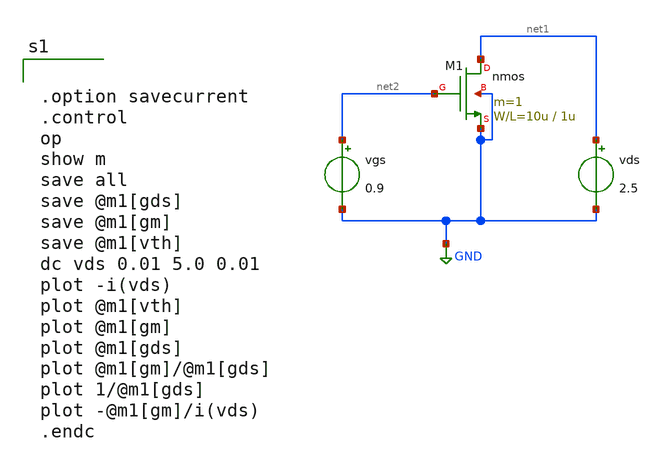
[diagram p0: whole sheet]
** sch_path: member_project/GroupWork/Team_masahiro/nfet_id-vds.sch
**.subckt nfet_id-vds
vgs net2 GND 0.9
vds net1 GND 2.5
M1 net1 net2 GND GND nmos L=1u W=10u m=1
**** begin user architecture code
 .include $::LIB/mos.lib
.include $::LIB/passive.lib
.include $::LIB/diode.lib


.option savecurrent
.control
op
show m
save all
save @m1[gds]
save @m1[gm]
save @m1[vth]
dc vds 0.01 5.0 0.01
plot -i(vds)
plot @m1[vth]
plot @m1[gm]
plot @m1[gds]
plot @m1[gm]/@m1[gds]
plot 1/@m1[gds]
plot -@m1[gm]/i(vds)
.endc


**** end user architecture code
**.ends
.GLOBAL GND
.end
